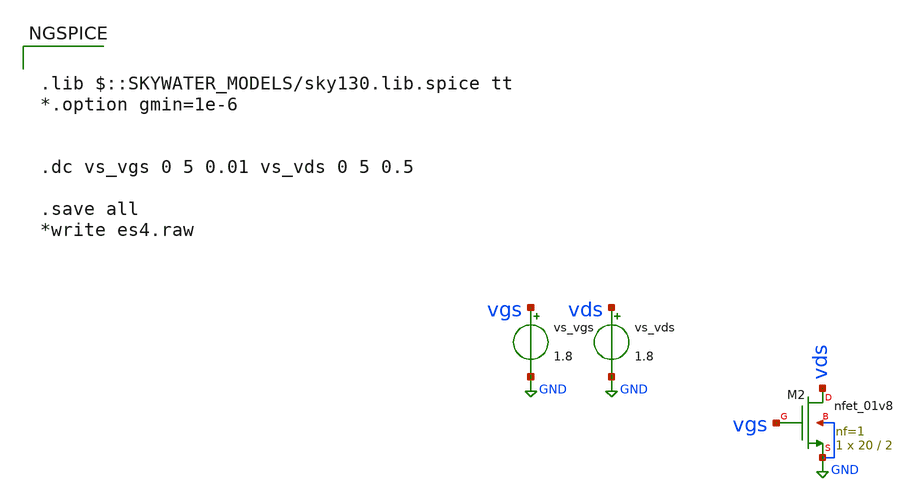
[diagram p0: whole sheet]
** sch_path: xschem/untitled.sch
**.subckt untitled
XM2 vds vgs GND GND sky130_fd_pr__nfet_01v8 L=2 W=20 nf=1 ad='int((1 + 1)/2) * 20 / 1 * 0.29' as='int((1 + 2)/2) * 20 / 1 * 0.29'
+ pd='2*int((1 + 1)/2) * (20 / 1 + 0.29)' ps='2*int((1 + 2)/2) * (20 / 1 + 0.29)' nrd='0.29 / 20 ' nrs='0.29 / 20 '
+ sa=0 sb=0 sd=0 mult=1 m=1
vs_vgs vgs GND 1.8
.save i(vs_vgs)
vs_vds vds GND 1.8
.save i(vs_vds)
**** begin user architecture code


.lib $::SKYWATER_MODELS/sky130.lib.spice tt
*.option gmin=1e-6


.dc vs_vgs 0 5 0.01 vs_vds 0 5 0.5

.save all
*write es4.raw




** opencircuitdesign pdks install
.lib $::SKYWATER_MODELS/sky130.lib.spice tt


**** end user architecture code
**.ends
.GLOBAL GND
.end
